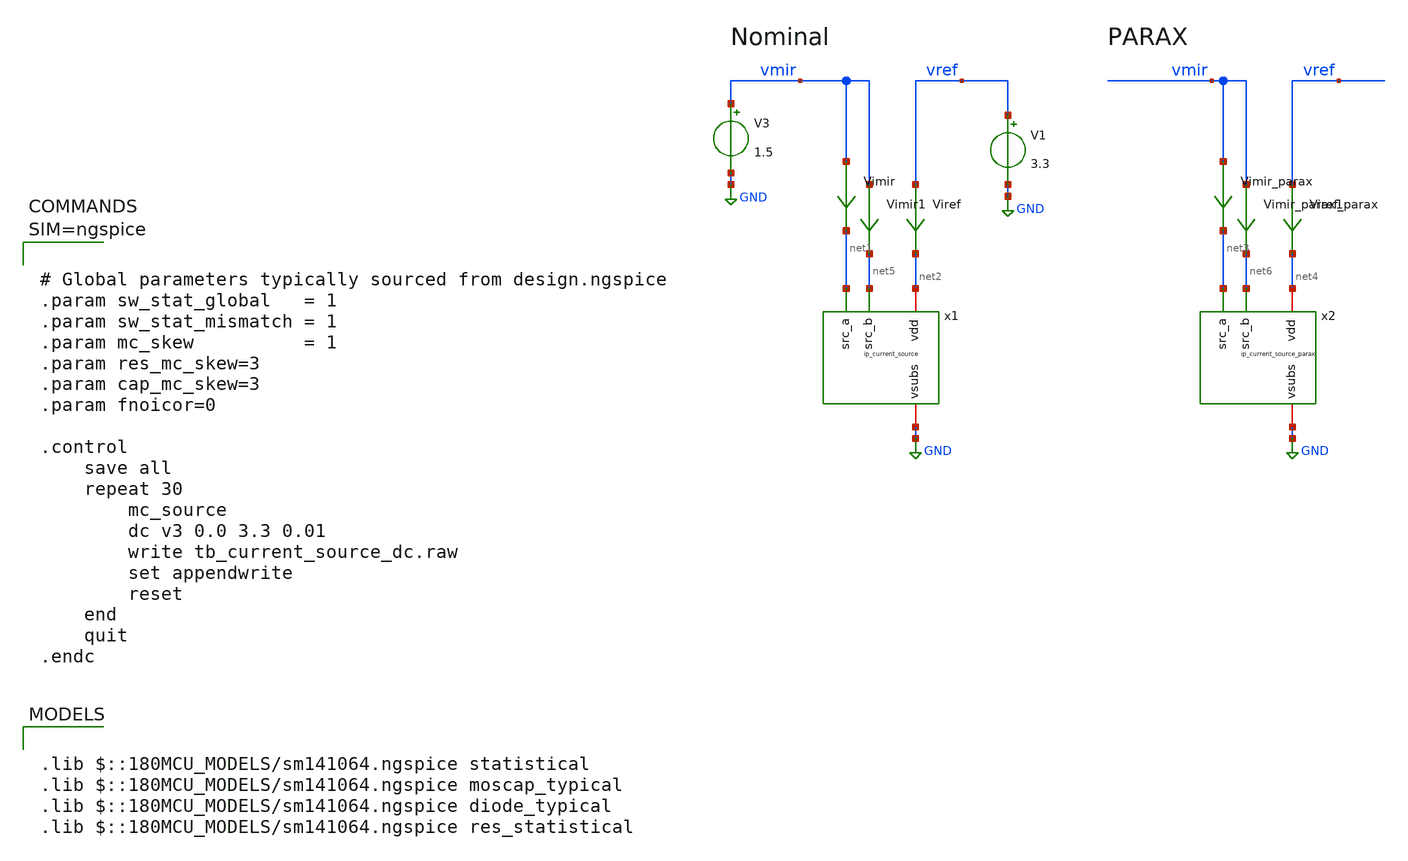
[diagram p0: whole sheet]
** sch_path: xschem/tb_current_source_dc.sch
**.subckt tb_current_source_dc
x1 net2 net1 GND net5 ip_current_source
V1 vref GND 3.3
V3 vmir GND 1.5
x2 net4 net3 GND net6 ip_current_source_parax
Vimir vmir net1 0
Viref vref net2 0
Vimir_parax vmir net3 0
Viref_parax vref net4 0
Vimir1 vmir net5 0
Vimir_parax1 vmir net6 0
**** begin user architecture code

.lib $::180MCU_MODELS/sm141064.ngspice statistical
.lib $::180MCU_MODELS/sm141064.ngspice moscap_typical
.lib $::180MCU_MODELS/sm141064.ngspice diode_typical
.lib $::180MCU_MODELS/sm141064.ngspice res_statistical




# Global parameters typically sourced from design.ngspice
.param sw_stat_global   = 1
.param sw_stat_mismatch = 1
.param mc_skew          = 1
.param res_mc_skew=3
.param cap_mc_skew=3
.param fnoicor=0

.control
	save all
	repeat 30
		mc_source
		dc v3 0.0 3.3 0.01
		write tb_current_source_dc.raw
		set appendwrite
		reset
	end
	quit
.endc



**** end user architecture code
**.ends

* expanding   symbol:  ip_current_source.sym # of pins=4
** sym_path: xschem/ip_current_source.sym
** sch_path: xschem/ip_current_source.sch
.subckt ip_current_source vdd src_a vsubs src_b
*.iopin vdd
*.iopin vsubs
*.ipin src_a
*.ipin src_b
XM8 refin refin vsubs vsubs nfet_06v0 L=1u W=5u nf=1 ad='int((nf+1)/2) * W/nf * 0.18u' as='int((nf+2)/2) * W/nf * 0.18u'
+ pd='2*int((nf+1)/2) * (W/nf + 0.18u)' ps='2*int((nf+2)/2) * (W/nf + 0.18u)' nrd='0.18u / W' nrs='0.18u / W'
+ sa=0 sb=0 sd=0 m=1 par=1
XM5 src_a refin net1 vsubs nfet_06v0 L=0.7u W=5u nf=1 ad='int((nf+1)/2) * W/nf * 0.18u' as='int((nf+2)/2) * W/nf * 0.18u'
+ pd='2*int((nf+1)/2) * (W/nf + 0.18u)' ps='2*int((nf+2)/2) * (W/nf + 0.18u)' nrd='0.18u / W' nrs='0.18u / W'
+ sa=0 sb=0 sd=0 m=1 par=1
XM2 src_a refin net1 vsubs nfet_06v0 L=0.7u W=5u nf=1 ad='int((nf+1)/2) * W/nf * 0.18u' as='int((nf+2)/2) * W/nf * 0.18u'
+ pd='2*int((nf+1)/2) * (W/nf + 0.18u)' ps='2*int((nf+2)/2) * (W/nf + 0.18u)' nrd='0.18u / W' nrs='0.18u / W'
+ sa=0 sb=0 sd=0 m=1 par=1
XM3 src_b refin net8 vsubs nfet_06v0 L=0.7u W=5u nf=1 ad='int((nf+1)/2) * W/nf * 0.18u' as='int((nf+2)/2) * W/nf * 0.18u'
+ pd='2*int((nf+1)/2) * (W/nf + 0.18u)' ps='2*int((nf+2)/2) * (W/nf + 0.18u)' nrd='0.18u / W' nrs='0.18u / W'
+ sa=0 sb=0 sd=0 m=1 par=1
XM6 src_b refin net8 vsubs nfet_06v0 L=0.7u W=5u nf=1 ad='int((nf+1)/2) * W/nf * 0.18u' as='int((nf+2)/2) * W/nf * 0.18u'
+ pd='2*int((nf+1)/2) * (W/nf + 0.18u)' ps='2*int((nf+2)/2) * (W/nf + 0.18u)' nrd='0.18u / W' nrs='0.18u / W'
+ sa=0 sb=0 sd=0 m=1 par=1
XM4 net1 refin vsubs vsubs nfet_06v0 L=5u W=0.5u nf=1 ad='int((nf+1)/2) * W/nf * 0.18u' as='int((nf+2)/2) * W/nf * 0.18u'
+ pd='2*int((nf+1)/2) * (W/nf + 0.18u)' ps='2*int((nf+2)/2) * (W/nf + 0.18u)' nrd='0.18u / W' nrs='0.18u / W'
+ sa=0 sb=0 sd=0 m=1 par=1
XM7 net8 refin vsubs vsubs nfet_06v0 L=5u W=0.5u nf=1 ad='int((nf+1)/2) * W/nf * 0.18u' as='int((nf+2)/2) * W/nf * 0.18u'
+ pd='2*int((nf+1)/2) * (W/nf + 0.18u)' ps='2*int((nf+2)/2) * (W/nf + 0.18u)' nrd='0.18u / W' nrs='0.18u / W'
+ sa=0 sb=0 sd=0 m=1 par=1
XR3 net2 net4 vsubs ppolyf_u_1k_6p0 r_width=1e-6 r_length=6e-6 m=1
XR4 net3 net2 vsubs ppolyf_u_1k_6p0 r_width=1e-6 r_length=6e-6 m=1
XR5 refin net3 vsubs ppolyf_u_1k_6p0 r_width=1e-6 r_length=6e-6 m=1
XR1 net4 net6 vsubs ppolyf_u_1k_6p0 r_width=1e-6 r_length=6e-6 m=1
XR2 net6 net5 vsubs ppolyf_u_1k_6p0 r_width=1e-6 r_length=6e-6 m=1
XR6 net5 net7 vsubs ppolyf_u_1k_6p0 r_width=1e-6 r_length=6e-6 m=1
XR7 net7 net10 vsubs ppolyf_u_1k_6p0 r_width=1e-6 r_length=2e-6 m=1
XR8 net10 net9 vsubs ppolyf_u_1k_6p0 r_width=1e-6 r_length=2e-6 m=1
XR9 net9 vdd vsubs ppolyf_u_1k_6p0 r_width=1e-6 r_length=2e-6 m=1
.ends


* expanding   symbol:  ip_current_source_parax.sym # of pins=4
** sym_path: xschem/ip_current_source.sym
.include [file normalize ../mag/ip_current_source.sim.spice]
.GLOBAL GND
.end
